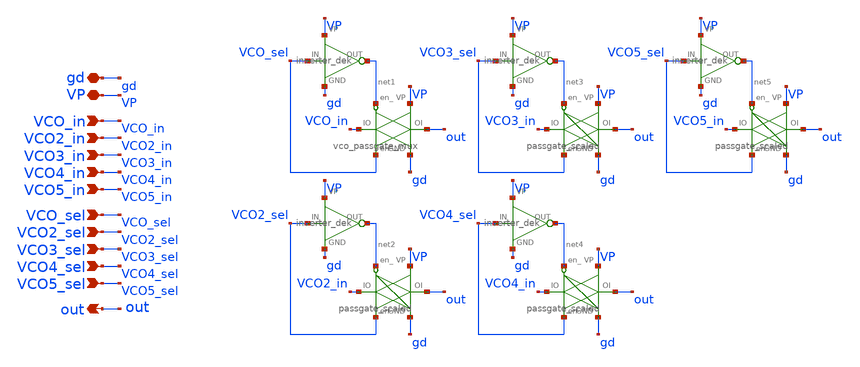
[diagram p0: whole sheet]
** sch_path: PLL0663-main/schematic/xschem/divider/VCO_MUX.sch
**.subckt VCO_MUX gd VP VCO2_in VCO3_in VCO4_in VCO5_in out VCO_in VCO2_sel VCO3_sel VCO_sel
*+ VCO4_sel VCO5_sel
*.iopin gd
*.iopin VP
*.ipin VCO2_in
*.ipin VCO3_in
*.ipin VCO4_in
*.ipin VCO5_in
*.opin out
*.ipin VCO_in
*.ipin VCO2_sel
*.ipin VCO3_sel
*.ipin VCO_sel
*.ipin VCO4_sel
*.ipin VCO5_sel
x2 VCO_sel net1 VP gd inverter_dek
x3 net2 VP gd VCO2_sel VCO2_in out passgate_scaled
x4 VCO2_sel net2 VP gd inverter_dek
x5 net3 VP gd VCO3_sel VCO3_in out passgate_scaled
x6 VCO3_sel net3 VP gd inverter_dek
x7 net4 VP gd VCO4_sel VCO4_in out passgate_scaled
x8 VCO4_sel net4 VP gd inverter_dek
x9 net5 VP gd VCO5_sel VCO5_in out passgate_scaled
x10 VCO5_sel net5 VP gd inverter_dek
x1 net1 VP gd VCO_sel VCO_in out vco_passgate_mux
**.ends
.end
